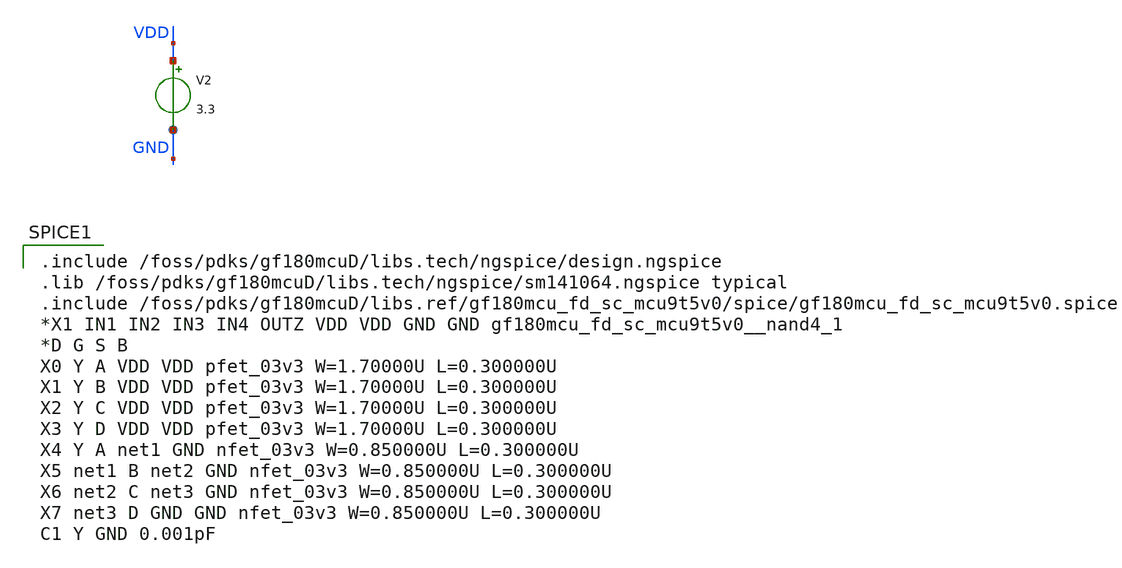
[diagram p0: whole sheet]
** sch_path: designs/libs/tb_NAND4/nand4_test_pow.sch
**.subckt nand4_test_pow
V2 VDD GND 3.3
**** begin user architecture code


*Vin1 A 0 PULSE(0 3.3 1n 10p 10p 10n 20n)
Vin1 A 0 DC 0
Vin2 B 0 DC 3.3
Vin3 C 0 DC 3.3
Vin4 D 0 DC 3.3

*.tran 10p 50n
.save all



.control
run print i_leak
tran 1p 5n
meas tran leakA avg I(V2) from=0n to=4n
let pleak=leakA*3.3
print pleak
*print I(V2)*V(V2)
*echo 'The tplh value for A NAND2_1 is: $&tplh_A' > /foss/designs/NAND4/schematic/NAND2_1_propagation.txt
*echo 'The tphl value for A NAND2_1 is: $&tphl_A' >> /foss/designs/NAND4/schematic/NAND2_1_propagation.txt
.endc




.include /foss/pdks/gf180mcuD/libs.tech/ngspice/design.ngspice
.lib /foss/pdks/gf180mcuD/libs.tech/ngspice/sm141064.ngspice typical
.include /foss/pdks/gf180mcuD/libs.ref/gf180mcu_fd_sc_mcu9t5v0/spice/gf180mcu_fd_sc_mcu9t5v0.spice
*X1 IN1 IN2 IN3 IN4 OUTZ VDD VDD GND GND gf180mcu_fd_sc_mcu9t5v0__nand4_1
*D G S B
X0 Y A VDD VDD pfet_03v3 W=1.70000U L=0.300000U
X1 Y B VDD VDD pfet_03v3 W=1.70000U L=0.300000U
X2 Y C VDD VDD pfet_03v3 W=1.70000U L=0.300000U
X3 Y D VDD VDD pfet_03v3 W=1.70000U L=0.300000U
X4 Y A net1 GND nfet_03v3 W=0.850000U L=0.300000U
X5 net1 B net2 GND nfet_03v3 W=0.850000U L=0.300000U
X6 net2 C net3 GND nfet_03v3 W=0.850000U L=0.300000U
X7 net3 D GND GND nfet_03v3 W=0.850000U L=0.300000U
C1 Y GND 0.001pF




**** end user architecture code
**.ends
.end
